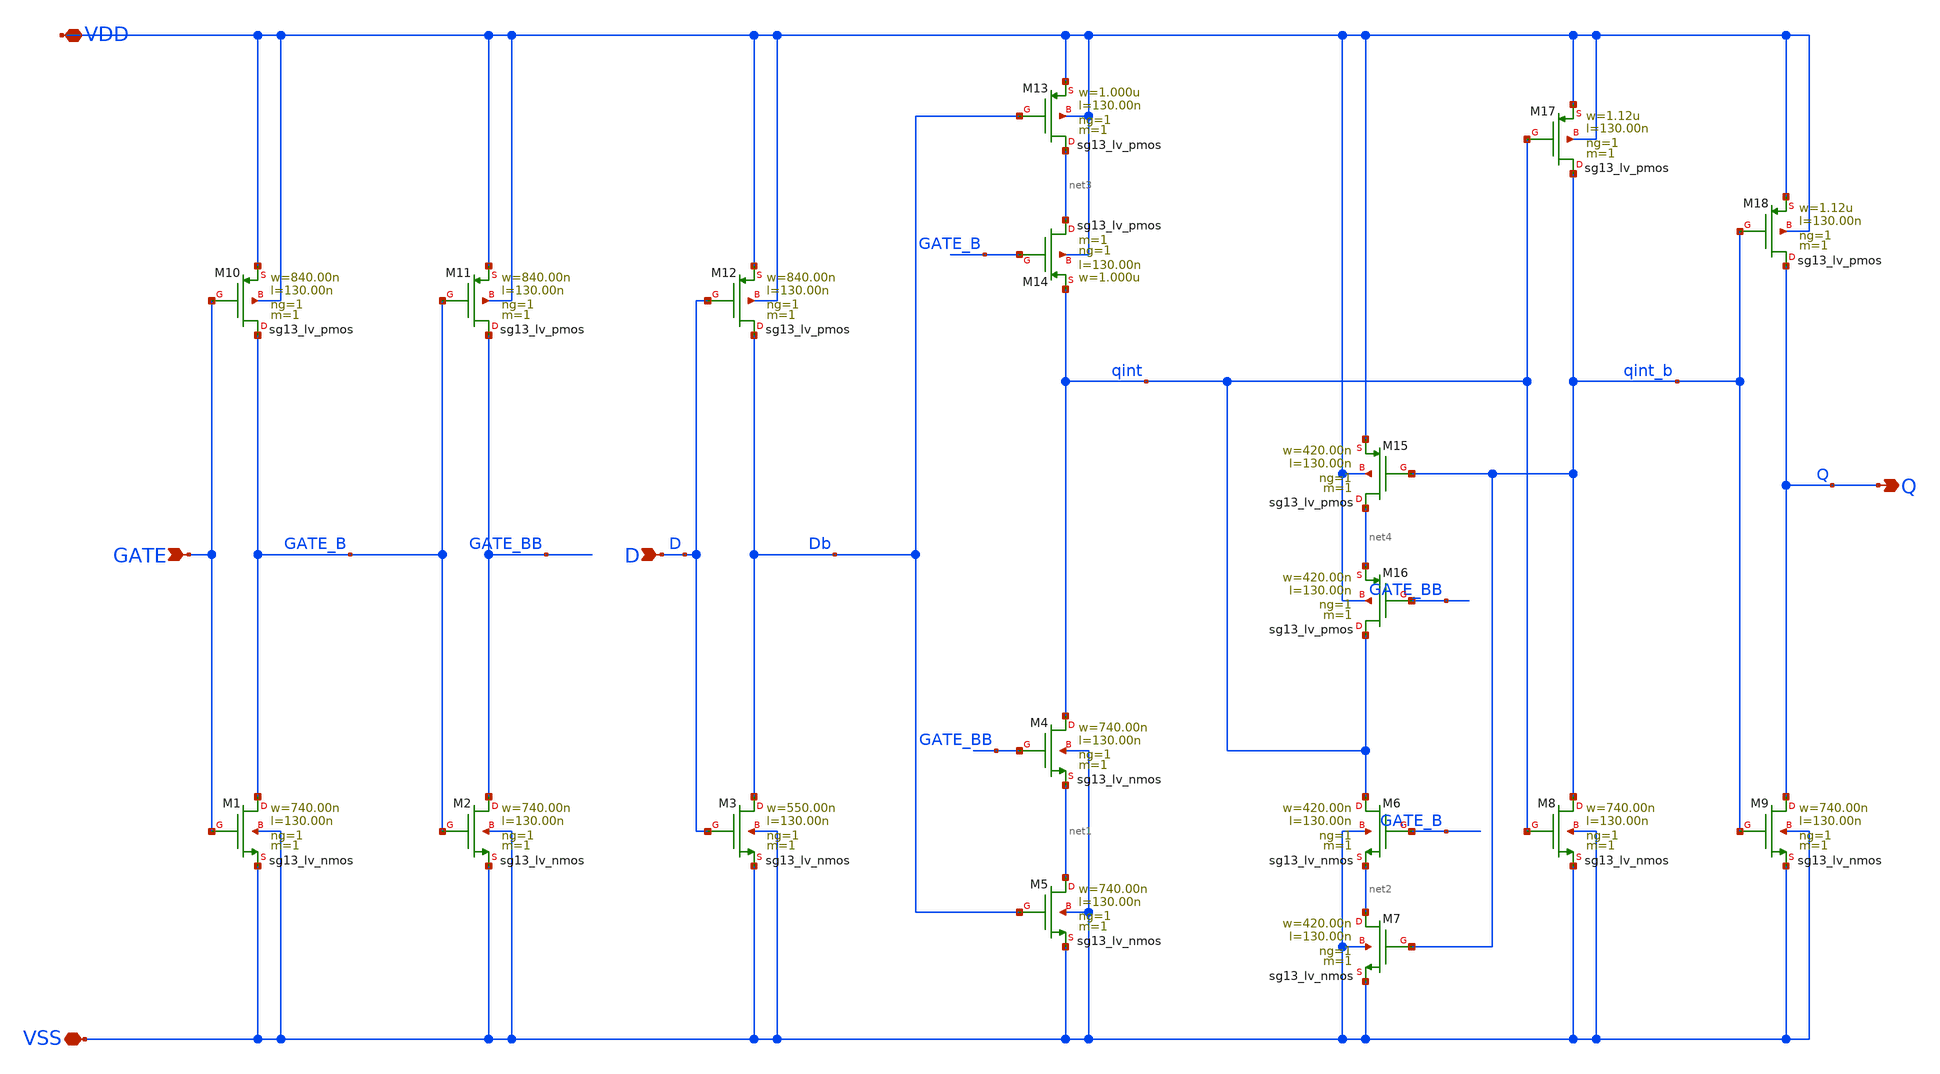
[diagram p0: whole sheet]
** sch_path: ihp-sg13g2/libs.tech/xschem/sg13g2_stdcells/sg13g2_dlhq_1.sch
* Copyright 2023 IHP PDK Authors
* Licensed under the Apache License, Version 2.0 (the "License");
* you may not use this file except in compliance with the License.
* You may obtain a copy of the License at
* https://www.apache.org/licenses/LICENSE-2.0
* Unless required by applicable law or agreed to in writing, software
* distributed under the License is distributed on an "AS IS" BASIS,
* WITHOUT WARRANTIES OR CONDITIONS OF ANY KIND, either express or implied.
* See the License for the specific language governing permissions and
* limitations under the License.
**.subckt sg13g2_dlhq_1 Q GATE D VDD VSS
*.opin Q
*.ipin GATE
*.ipin D
*.iopin VDD
*.iopin VSS
XM1 GATE_B GATE VSS VSS sg13_lv_nmos w=740.00n l=130.00n ng=1 m=1 mm_ok=1
XM2 GATE_BB GATE_B VSS VSS sg13_lv_nmos w=740.00n l=130.00n ng=1 m=1 mm_ok=1
XM3 Db D VSS VSS sg13_lv_nmos w=550.00n l=130.00n ng=1 m=1 mm_ok=1
XM4 qint GATE_BB net1 VSS sg13_lv_nmos w=740.00n l=130.00n ng=1 m=1 mm_ok=1
XM5 net1 Db VSS VSS sg13_lv_nmos w=740.00n l=130.00n ng=1 m=1 mm_ok=1
XM6 qint GATE_B net2 VSS sg13_lv_nmos w=420.00n l=130.00n ng=1 m=1 mm_ok=1
XM7 net2 qint_b VSS VSS sg13_lv_nmos w=420.00n l=130.00n ng=1 m=1 mm_ok=1
XM8 qint_b qint VSS VSS sg13_lv_nmos w=740.00n l=130.00n ng=1 m=1 mm_ok=1
XM9 Q qint_b VSS VSS sg13_lv_nmos w=740.00n l=130.00n ng=1 m=1 mm_ok=1
XM10 GATE_B GATE VDD VDD sg13_lv_pmos w=840.00n l=130.00n ng=1 m=1 mm_ok=1
XM11 GATE_BB GATE_B VDD VDD sg13_lv_pmos w=840.00n l=130.00n ng=1 m=1 mm_ok=1
XM12 Db D VDD VDD sg13_lv_pmos w=840.00n l=130.00n ng=1 m=1 mm_ok=1
XM13 net3 Db VDD VDD sg13_lv_pmos w=1.000u l=130.00n ng=1 m=1 mm_ok=1
XM14 net3 GATE_B qint VDD sg13_lv_pmos w=1.000u l=130.00n ng=1 m=1 mm_ok=1
XM15 net4 qint_b VDD VDD sg13_lv_pmos w=420.00n l=130.00n ng=1 m=1 mm_ok=1
XM16 qint GATE_BB net4 VDD sg13_lv_pmos w=420.00n l=130.00n ng=1 m=1 mm_ok=1
XM17 qint_b qint VDD VDD sg13_lv_pmos w=1.12u l=130.00n ng=1 m=1 mm_ok=1
XM18 Q qint_b VDD VDD sg13_lv_pmos w=1.12u l=130.00n ng=1 m=1 mm_ok=1
**.ends
.end
